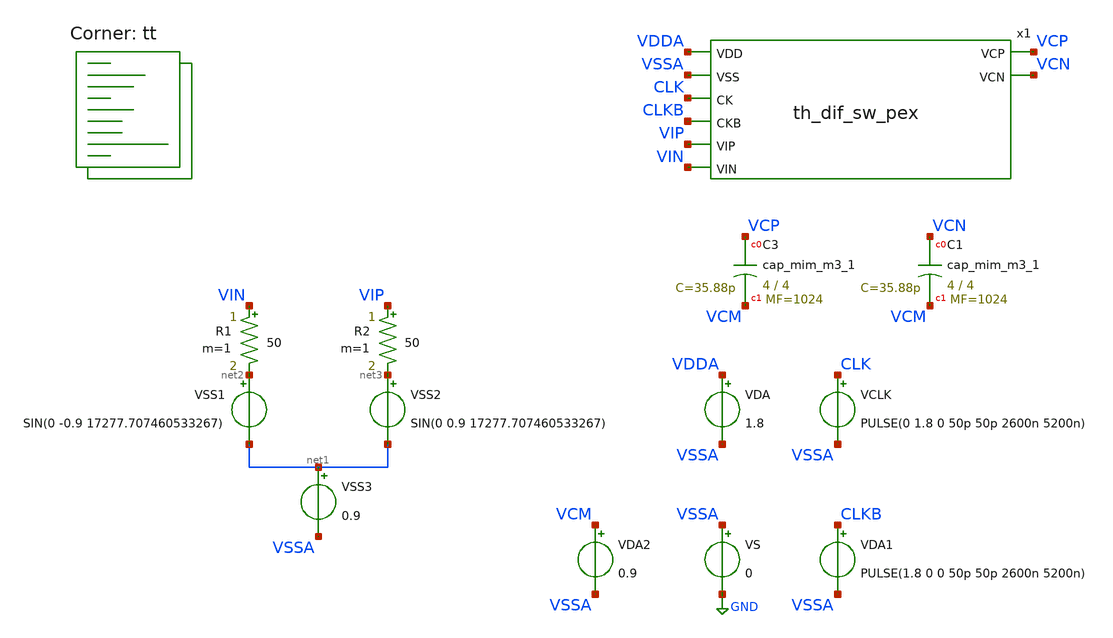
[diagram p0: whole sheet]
** sch_path: xschem/th_tb.sch
**.subckt th_tb
VS VSSA GND 0
VDA VDDA VSSA 1.8
VSS3 net1 VSSA 0.9
VCLK CLK VSSA PULSE(0 1.8 0 50p 50p 2600n 5200n)
R1 VIN net2 50 m=1
R2 VIP net3 50 m=1
VDA1 CLKB VSSA PULSE(1.8 0 0 50p 50p 2600n 5200n)
x1 VDDA VSSA CLK CLKB VIP VIN VCP VCN th_dif_sw_pex
VDA2 VCM VSSA 0.9
XC3 VCP VCM sky130_fd_pr__cap_mim_m3_1 W=4 L=4 MF=1024 m=1024
XC1 VCN VCM sky130_fd_pr__cap_mim_m3_1 W=4 L=4 MF=1024 m=1024
VSS1 net2 net1 SIN(0 -0.9 17277.707460533267)
VSS2 net3 net1 SIN(0 0.9 17277.707460533267)
**** begin user architecture code


.option wnflag=0 bypass=1
.options method=trap rawfile=binary
.options solver=klu nomod
.control
set num_threads=6
save CLK CLKB VIP VIN VCP VCN
global netlist_dir .
set wr_singlescale
tran 1n 5350u  ; Mengubah start time menjadi 1n
remzerovec
write th_tb_pex.raw
wrdata th_tb_pex.txt CLK CLKB VIP VIN VCP VCN
quit 0
.endc

.lib $::SKYWATER_MODELS/sky130.lib.spice tt

** opencircuitdesign pdks install
* .lib $::SKYWATER_MODELS/sky130.lib.spice tt
*.include $PDK_ROOT/$PDK/libs.ref/sky130_fd_sc_hdll/spice/sky130_fd_sc_hdll.spice
.include $PDK_ROOT/$PDK/libs.ref/sky130_fd_sc_hs/spice/sky130_fd_sc_hs.spice
*.include $PDK_ROOT/$PDK/libs.ref/sky130_fd_sc_hd/spice/sky130_fd_sc_hd.spice

**** end user architecture code
**.ends

* expanding   symbol:  th_dif_sw_pex.sym # of pins=8
** sym_path: xschem/th_dif_sw_pex.sym
.include /home/mthudaa/vlsi/8bit_SAR-ADC_ITS/xschem/th_dif_sw_pex.spice
.GLOBAL GND
.end
